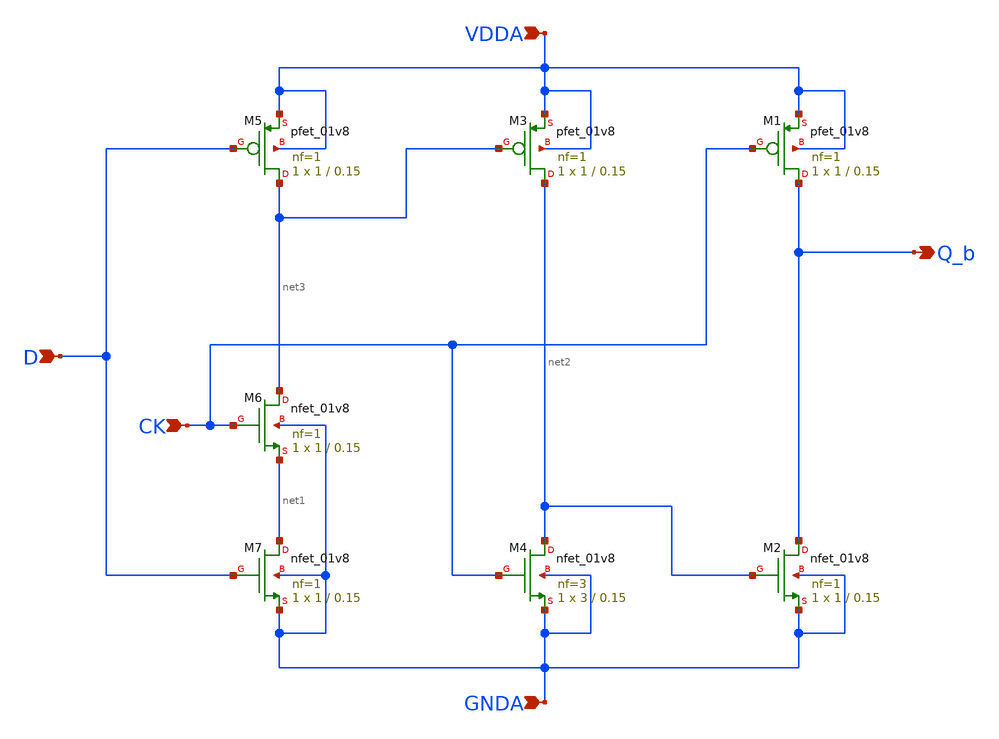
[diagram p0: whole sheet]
** sch_path: projects/pll/divider/xschem_ngspice/TSPC_FF_ratioed.sch
**.subckt TSPC_FF_ratioed CK D Q_b VDDA GNDA
*.ipin CK
*.ipin D
*.opin Q_b
*.ipin VDDA
*.ipin GNDA
XM1 Q_b CK VDDA VDDA sky130_fd_pr__pfet_01v8 L=0.15 W=1 nf=1 ad='int((nf+1)/2) * W/nf * 0.29' as='int((nf+2)/2) * W/nf * 0.29'
+ pd='2*int((nf+1)/2) * (W/nf + 0.29)' ps='2*int((nf+2)/2) * (W/nf + 0.29)' nrd='0.29 / W' nrs='0.29 / W'
+ sa=0 sb=0 sd=0 mult=1 m=1
XM2 Q_b net2 GNDA GNDA sky130_fd_pr__nfet_01v8 L=0.15 W=1 nf=1 ad='int((nf+1)/2) * W/nf * 0.29' as='int((nf+2)/2) * W/nf * 0.29'
+ pd='2*int((nf+1)/2) * (W/nf + 0.29)' ps='2*int((nf+2)/2) * (W/nf + 0.29)' nrd='0.29 / W' nrs='0.29 / W'
+ sa=0 sb=0 sd=0 mult=1 m=1
XM3 net2 net3 VDDA VDDA sky130_fd_pr__pfet_01v8 L=0.15 W=1 nf=1 ad='int((nf+1)/2) * W/nf * 0.29' as='int((nf+2)/2) * W/nf * 0.29'
+ pd='2*int((nf+1)/2) * (W/nf + 0.29)' ps='2*int((nf+2)/2) * (W/nf + 0.29)' nrd='0.29 / W' nrs='0.29 / W'
+ sa=0 sb=0 sd=0 mult=1 m=1
XM4 net2 CK GNDA GNDA sky130_fd_pr__nfet_01v8 L=0.15 W=3 nf=3 ad='int((nf+1)/2) * W/nf * 0.29' as='int((nf+2)/2) * W/nf * 0.29'
+ pd='2*int((nf+1)/2) * (W/nf + 0.29)' ps='2*int((nf+2)/2) * (W/nf + 0.29)' nrd='0.29 / W' nrs='0.29 / W'
+ sa=0 sb=0 sd=0 mult=1 m=1
XM5 net3 D VDDA VDDA sky130_fd_pr__pfet_01v8 L=0.15 W=1 nf=1 ad='int((nf+1)/2) * W/nf * 0.29' as='int((nf+2)/2) * W/nf * 0.29'
+ pd='2*int((nf+1)/2) * (W/nf + 0.29)' ps='2*int((nf+2)/2) * (W/nf + 0.29)' nrd='0.29 / W' nrs='0.29 / W'
+ sa=0 sb=0 sd=0 mult=1 m=1
XM7 net1 D GNDA GNDA sky130_fd_pr__nfet_01v8 L=0.15 W=1 nf=1 ad='int((nf+1)/2) * W/nf * 0.29' as='int((nf+2)/2) * W/nf * 0.29'
+ pd='2*int((nf+1)/2) * (W/nf + 0.29)' ps='2*int((nf+2)/2) * (W/nf + 0.29)' nrd='0.29 / W' nrs='0.29 / W'
+ sa=0 sb=0 sd=0 mult=1 m=1
XM6 net3 CK net1 GNDA sky130_fd_pr__nfet_01v8 L=0.15 W=1 nf=1 ad='int((nf+1)/2) * W/nf * 0.29' as='int((nf+2)/2) * W/nf * 0.29'
+ pd='2*int((nf+1)/2) * (W/nf + 0.29)' ps='2*int((nf+2)/2) * (W/nf + 0.29)' nrd='0.29 / W' nrs='0.29 / W'
+ sa=0 sb=0 sd=0 mult=1 m=1
**.ends
.end
